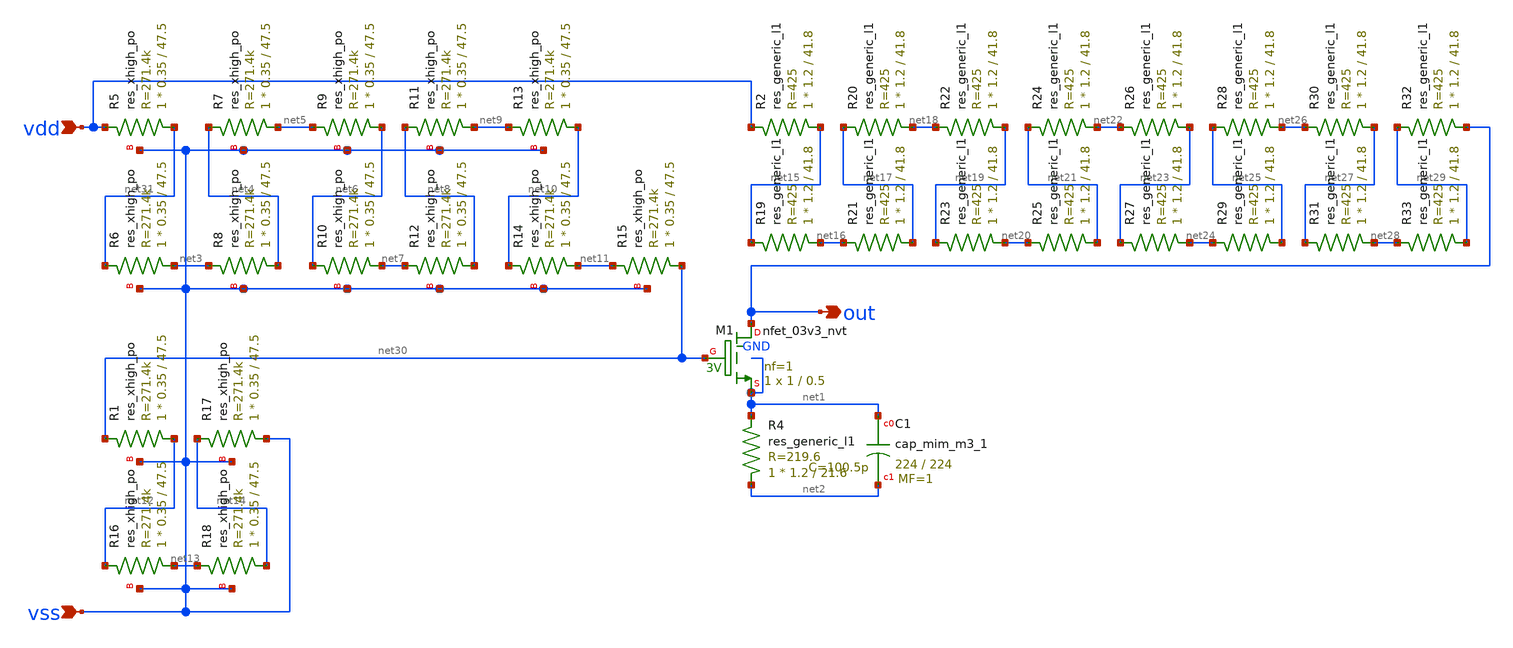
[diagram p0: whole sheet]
** sch_path: voltagedivider.sch
**.subckt voltagedivider vdd vss out
*.ipin vdd
*.ipin vss
*.opin out
XC1 net1 net2 sky130_fd_pr__cap_mim_m3_1 W=224 L=224 MF=1 m=1
R4 net2 net1 sky130_fd_pr__res_generic_l1 W=1.2 L=21.6 m=1
XM1 out net30 net1 GND sky130_fd_pr__nfet_03v3_nvt L=0.5 W=1 nf=1 ad='int((1 + 1)/2) * 1 / 1 * 0.29'
+ as='int((1 + 2)/2) * 1 / 1 * 0.29' pd='2*int((1 + 1)/2) * (1 / 1 + 0.29)' ps='2*int((1 + 2)/2) * (1 / 1 + 0.29)'
+ nrd='0.29 / 1 ' nrs='0.29 / 1 ' sa=0 sb=0 sd=0 mult=1 m=1
XR5 net31 vdd vss sky130_fd_pr__res_xhigh_po W=0.35 L=47.5 mult=1 m=1
XR1 net12 net30 vss sky130_fd_pr__res_xhigh_po W=0.35 L=47.5 mult=1 m=1
R2 net15 vdd sky130_fd_pr__res_generic_l1 W=1.2 L=41.8 m=1
XR6 net3 net31 vss sky130_fd_pr__res_xhigh_po W=0.35 L=47.5 mult=1 m=1
XR7 net5 net4 vss sky130_fd_pr__res_xhigh_po W=0.35 L=47.5 mult=1 m=1
XR8 net4 net3 vss sky130_fd_pr__res_xhigh_po W=0.35 L=47.5 mult=1 m=1
XR9 net6 net5 vss sky130_fd_pr__res_xhigh_po W=0.35 L=47.5 mult=1 m=1
XR10 net7 net6 vss sky130_fd_pr__res_xhigh_po W=0.35 L=47.5 mult=1 m=1
XR11 net9 net8 vss sky130_fd_pr__res_xhigh_po W=0.35 L=47.5 mult=1 m=1
XR12 net8 net7 vss sky130_fd_pr__res_xhigh_po W=0.35 L=47.5 mult=1 m=1
XR13 net10 net9 vss sky130_fd_pr__res_xhigh_po W=0.35 L=47.5 mult=1 m=1
XR14 net11 net10 vss sky130_fd_pr__res_xhigh_po W=0.35 L=47.5 mult=1 m=1
XR15 net30 net11 vss sky130_fd_pr__res_xhigh_po W=0.35 L=47.5 mult=1 m=1
XR16 net13 net12 vss sky130_fd_pr__res_xhigh_po W=0.35 L=47.5 mult=1 m=1
XR17 vss net14 vss sky130_fd_pr__res_xhigh_po W=0.35 L=47.5 mult=1 m=1
XR18 net14 net13 vss sky130_fd_pr__res_xhigh_po W=0.35 L=47.5 mult=1 m=1
R19 net16 net15 sky130_fd_pr__res_generic_l1 W=1.2 L=41.8 m=1
R20 net18 net17 sky130_fd_pr__res_generic_l1 W=1.2 L=41.8 m=1
R21 net17 net16 sky130_fd_pr__res_generic_l1 W=1.2 L=41.8 m=1
R22 net19 net18 sky130_fd_pr__res_generic_l1 W=1.2 L=41.8 m=1
R23 net20 net19 sky130_fd_pr__res_generic_l1 W=1.2 L=41.8 m=1
R24 net22 net21 sky130_fd_pr__res_generic_l1 W=1.2 L=41.8 m=1
R25 net21 net20 sky130_fd_pr__res_generic_l1 W=1.2 L=41.8 m=1
R26 net23 net22 sky130_fd_pr__res_generic_l1 W=1.2 L=41.8 m=1
R27 net24 net23 sky130_fd_pr__res_generic_l1 W=1.2 L=41.8 m=1
R28 net26 net25 sky130_fd_pr__res_generic_l1 W=1.2 L=41.8 m=1
R29 net25 net24 sky130_fd_pr__res_generic_l1 W=1.2 L=41.8 m=1
R30 net27 net26 sky130_fd_pr__res_generic_l1 W=1.2 L=41.8 m=1
R31 net28 net27 sky130_fd_pr__res_generic_l1 W=1.2 L=41.8 m=1
R32 out net29 sky130_fd_pr__res_generic_l1 W=1.2 L=41.8 m=1
R33 net29 net28 sky130_fd_pr__res_generic_l1 W=1.2 L=41.8 m=1
**.ends
.end
